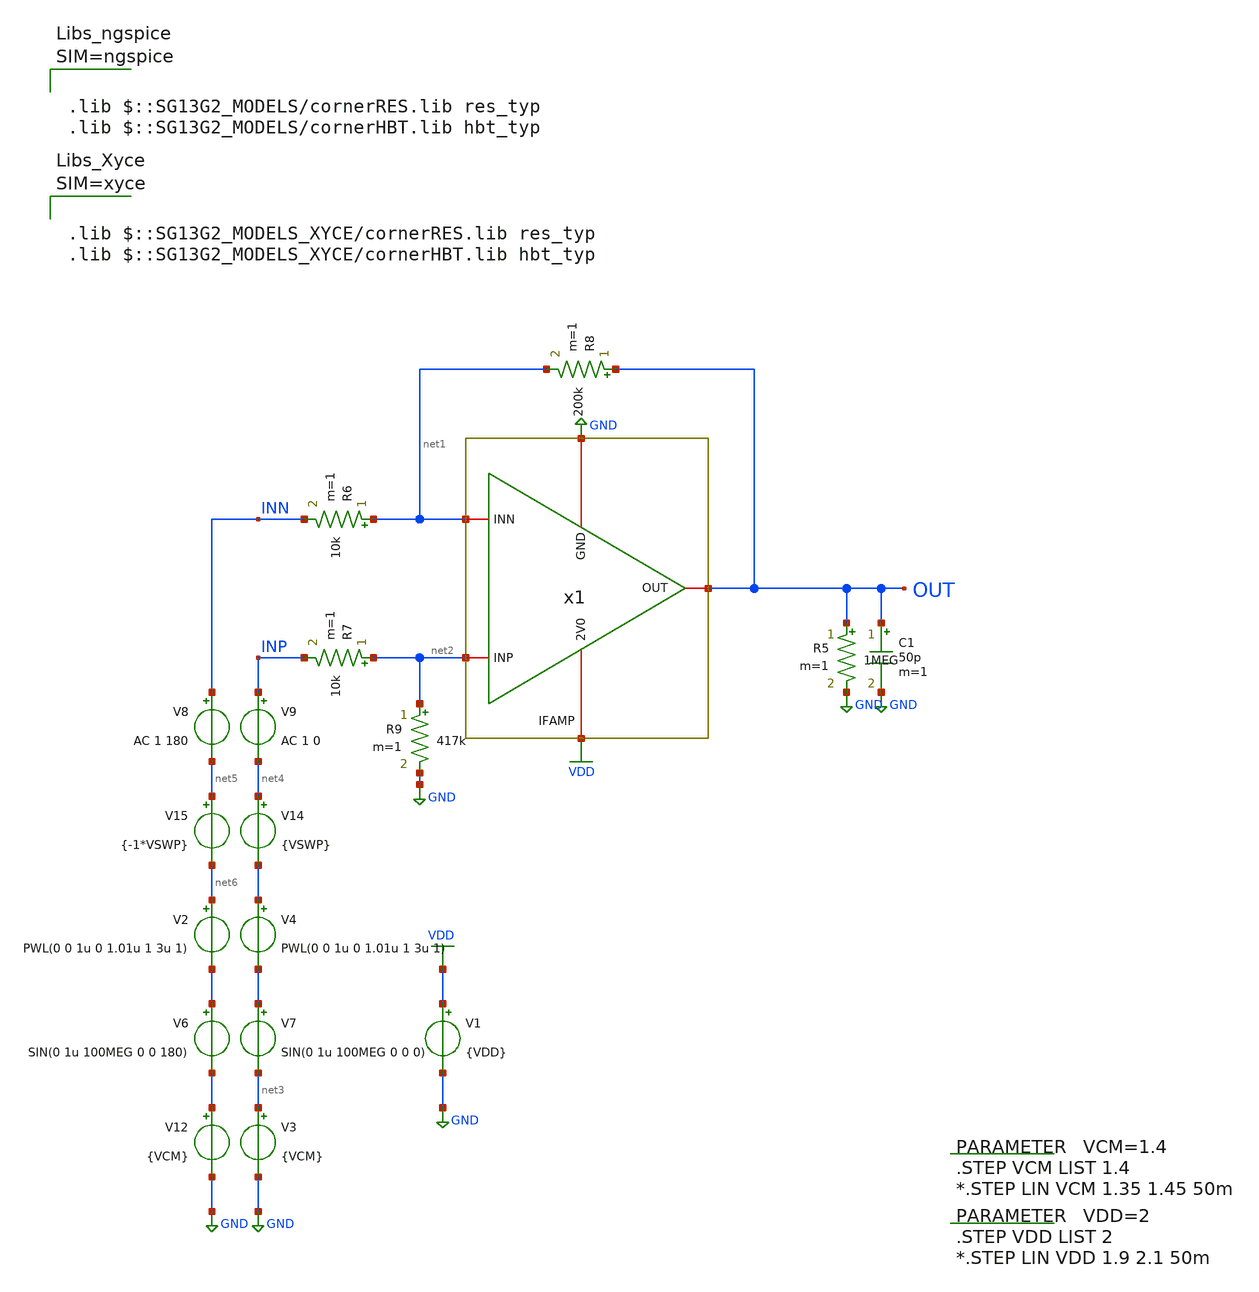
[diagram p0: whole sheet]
** sch_path: mWATTBAT/design_data/xschem/IFAMP_TB.sch
**.subckt IFAMP_TB
V1 VDD GND {VDD}
V8 INN net5 AC 1 180
V9 INP net4 AC 1 0
.param VDD=2
.STEP VDD LIST 2
*.STEP LIN VDD 1.9 2.1 50m
.param VCM=1.4
.STEP VCM LIST 1.4
*.STEP LIN VCM 1.35 1.45 50m
V3 net3 GND {VCM}
V12 net6 GND {VCM}
V14 net4 net3 {VSWP}
V15 net5 net6 {-1*VSWP}
x1 VDD net2 net1 OUT GND IFAMP
R5 OUT GND 1MEG m=1
R6 net1 INN 10k m=1
R7 net2 INP 10k m=1
R8 OUT net1 200k m=1
R9 net2 GND 417k m=1
C1 OUT GND 50p m=1
**** begin user architecture code


.PREPROCESS REPLACEGROUND TRUE
.PARAM VSWP=0
.DC LIN VSWP -100m 100m 100u
*.DC LIN V5 -100m 100m 100m
.MEAS DC IDD EQN {-1*I(V1)}
.PRINT DC FORMAT=RAW FILE=IFAMP_TBDC.raw V(*) I(*) VDD VCM IDD








.lib $::SG13G2_MODELS/cornerRES.lib res_typ
.lib $::SG13G2_MODELS/cornerHBT.lib hbt_typ



**** end user architecture code
**.ends

* expanding   symbol:  IFAMP.sym # of pins=5
** sym_path: mWATTBAT/design_data/xschem/IFAMP.sym
** sch_path: mWATTBAT/design_data/xschem/IFAMP.sch
.subckt IFAMP 2V0 INP INN OUT GND
*.iopin INP
*.iopin INN
*.iopin OUT
*.iopin 2V0
*.iopin GND
XM1 vs_1c INP vs_1_2 2V0 sg13_lv_pmos w=29u l=0.25u ng=29 m=1 mm_ok=1
XM2 vs_2c INN vs_1_2 2V0 sg13_lv_pmos w=29u l=0.25u ng=29 m=1 mm_ok=1
XM1C vg_3_4 vg_1c_2c vs_1c 2V0 sg13_lv_pmos w=4u l=0.25u ng=20 m=1 mm_ok=1
XM2C OUT1 vg_1c_2c vs_2c 2V0 sg13_lv_pmos w=4u l=0.25u ng=20 m=1 mm_ok=1
XM3C vg_3_4 vg_3c_4c vs_3c GND sg13_lv_nmos w=0.5u l=1u ng=2 m=1 mm_ok=1
XM4C OUT1 vg_3c_4c vs_4c GND sg13_lv_nmos w=0.5u l=1u ng=2 m=1 mm_ok=1
XM3 vs_3c vg_3_4 GND GND sg13_lv_nmos w=0.5u l=1u ng=1 m=1 mm_ok=1
XM4 vs_4c vg_3_4 GND GND sg13_lv_nmos w=0.5u l=1u ng=1 m=1 mm_ok=1
XM5 vs_1_2 vg_5_6 2V0 2V0 sg13_lv_pmos w=26.5u l=5u ng=20 m=1 mm_ok=1
XM6 vg_5_6 vg_5_6 2V0 2V0 sg13_lv_pmos w=13.25u l=5u ng=10 m=1 mm_ok=1
XM7 OUT OUT1 GND GND sg13_hv_nmos w=8.4u l=0.6u ng=14 m=1 mm_ok=1
XM8 OUT OUT1 2V0 2V0 sg13_hv_pmos w=0.6u l=0.6u ng=1 m=1 mm_ok=1
XM9 vg_3c_4c vg_3c_4c vs_1_2 2V0 sg13_lv_pmos w=0.84u l=6u ng=4 m=1 mm_ok=1
XM10 vg_3c_4c vg_3c_4c vg_1c_2c GND sg13_lv_nmos w=15u l=5u ng=20 m=1 mm_ok=1
XM11 vg_1c_2c vg_1c_2c GND GND sg13_lv_nmos w=0.4u l=6u ng=2 m=1 mm_ok=1
XM13 vg_13 vg_13 GND GND sg13_lv_nmos w=1.6u l=5u ng=8 m=1 mm_ok=1
XM12 vg_5_6 vg_5_6 vg_13 GND sg13_lv_nmos w=1.6u l=5u ng=8 m=1 mm_ok=1
**** begin user architecture code



**** end user architecture code
**** begin user architecture code



.lib $::SG13G2_MODELS/cornerMOSlv.lib mos_tt
.lib $::SG13G2_MODELS/cornerMOShv.lib mos_tt
.lib $::SG13G2_MODELS/cornerRES.lib res_typ
.lib $::SG13G2_MODELS/cornerHBT.lib hbt_typ



**** end user architecture code
XM13D VSS vg_13 VSS VSS sg13_lv_nmos w=2.6u l=5u ng=13 m=2 mm_ok=1
XM12D VSS vg_5_6 VSS VSS sg13_lv_nmos w=2.6u l=5u ng=13 m=2 mm_ok=1
XM6D VDD vg_5_6 VDD VDD sg13_lv_pmos w=15.9u l=5u ng=12 m=2 mm_ok=1
XM5D VDD vs_1_2 VDD VDD sg13_lv_pmos w=9.275u l=5u ng=7 m=2 mm_ok=1
XM11D VSS vg_1c_2c VSS VSS sg13_lv_nmos w=2.6u l=6u ng=13 m=2 mm_ok=1
XM9D VDD vg_3c_4c VDD VDD sg13_lv_pmos w=2.52u l=6u ng=12 m=2 mm_ok=1
XM10D VSS vg_3c_4c VSS VSS sg13_lv_nmos w=5.25u l=5u ng=7 m=2 mm_ok=1
XM3CD VSS vg_3c_4c VSS VSS sg13_lv_nmos w=15.25u l=1u ng=61 m=1 mm_ok=1
XM3D VSS VSS VSS VSS sg13_lv_nmos w=0.5u l=1u ng=1 m=86 mm_ok=1
XM4CD VSS vg_3c_4c VSS VSS sg13_lv_nmos w=15.25u l=1u ng=61 m=1 mm_ok=1
XM1CD VDD vg_1c_2c VDD VDD sg13_lv_pmos w=22u l=0.25u ng=110 m=1 mm_ok=1
XM2CD VDD vg_1c_2c VDD VDD sg13_lv_pmos w=22u l=0.25u ng=110 m=1 mm_ok=1
XM1D VDD vs_1_2 VDD VDD sg13_lv_pmos w=115u l=0.25u ng=115 m=1 mm_ok=1
XM2D VDD vs_1_2 VDD VDD sg13_lv_pmos w=115u l=0.25u ng=115 m=1 mm_ok=1
XM4D VSS VSS VSS VSS sg13_lv_nmos w=0.5u l=1u ng=1 m=86 mm_ok=1
XM7D VSS VDD VSS VSS sg13_hv_nmos w=8.4u l=0.6u ng=14 m=56 mm_ok=1
XM8D VDD VSS VDD VDD sg13_hv_pmos w=0.6u l=0.6u ng=1 m=56 mm_ok=1
XR21 OUT OUT1 sub! rppd w=2.21e-6 l=10.0e-6 m=1 b=67 mm_ok=1
.ends

.GLOBAL VDD
.GLOBAL GND
.end
